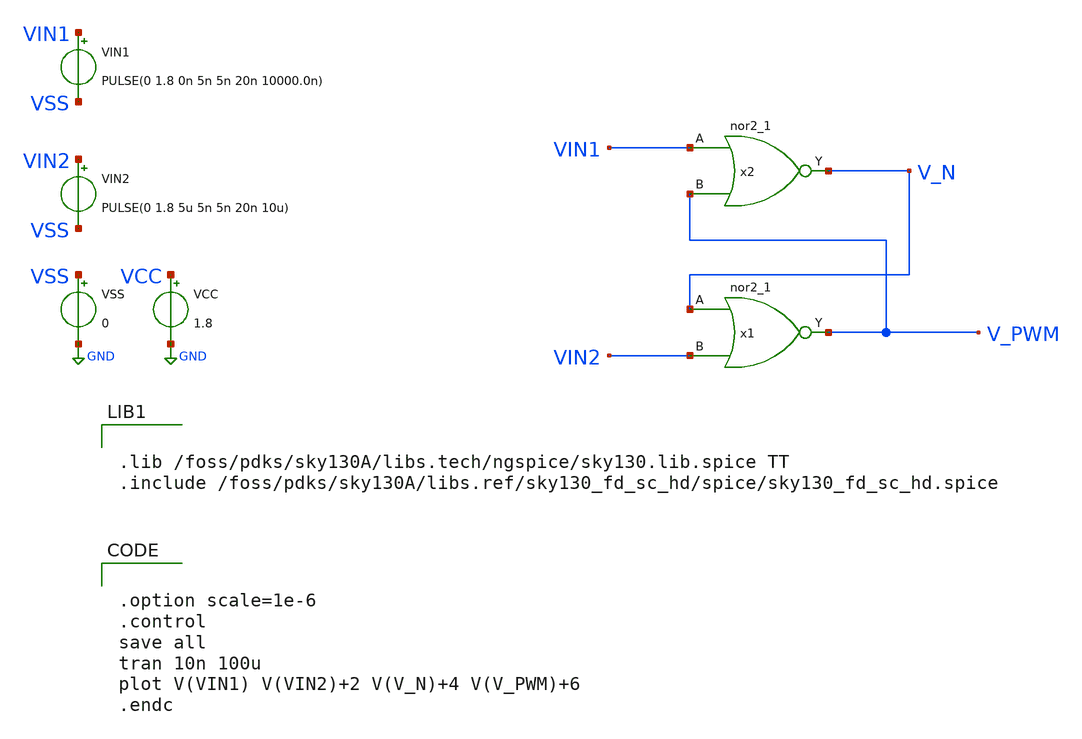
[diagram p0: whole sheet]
** sch_path: xschem/tb_SRlatch_NOR.sch
**.subckt tb_SRlatch_NOR
VCC VCC GND 1.8
VSS VSS GND 0
VIN2 VIN2 VSS PULSE(0 1.8 5u 5n 5n 20n 10u)
x2 VIN1 V_PWM VSS VSS VCC VCC V_N sky130_fd_sc_hd__nor2_1
x1 V_N VIN2 VSS VSS VCC VCC V_PWM sky130_fd_sc_hd__nor2_1
VIN1 VIN1 VSS PULSE(0 1.8 0n 5n 5n 20n 10000.0n)
**** begin user architecture code


.lib /foss/pdks/sky130A/libs.tech/ngspice/sky130.lib.spice TT
.include /foss/pdks/sky130A/libs.ref/sky130_fd_sc_hd/spice/sky130_fd_sc_hd.spice




.option scale=1e-6
.control
save all
tran 10n 100u
plot V(VIN1) V(VIN2)+2 V(V_N)+4 V(V_PWM)+6
.endc


**** end user architecture code
**.ends
.GLOBAL GND
.end
